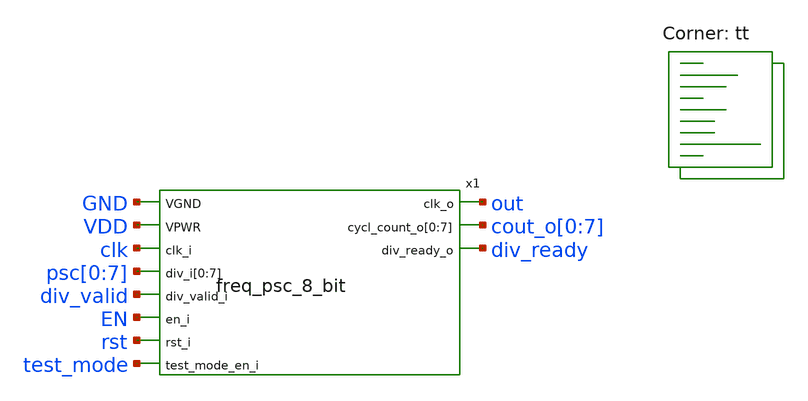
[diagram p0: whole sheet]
** sch_path: xschem/freq_psc_8_bit-tb.sch
**.subckt freq_psc_8_bit-tb
x1 GND VDD clk out cout_o[0] cout_o[1] cout_o[2] cout_o[3] cout_o[4] cout_o[5] cout_o[6] cout_o[7]
+ psc[0] psc[1] psc[2] psc[3] psc[4] psc[5] psc[6] psc[7] div_ready div_valid EN rst test_mode
+ freq_psc_8_bit
**** begin user architecture code



  .include ~/sky130_projects/sky130_its_biomedical_chip_research_2024/spice/clk_int_div.spice
  .param max_freq=100e6 period={1/max_freq} time_high={period/2}
  .param delay_vin1={time_high} delay_vin2={time_high*1.5}

  .option wnflag=1
  .option safecurrents

  Vvdd VDD GND dc 1.8
  Vrst rst GND pulse(0 1.8 {period*5} 1p 1p {time_high*5} {period*50})
  Vin1 clk GND pulse(0 1.8 {delay_vin1} 1p 1p {time_high} {period})

  Vdiv div_valid gnd pulse(0 1.8 {period*5} 1p 1p {period*50} {period*100})

  Vtest test_mode gnd dc 0
  Ven EN gnd dc 1.8

  Vpsc0  psc[0] gnd dc 0
  Vpsc1  psc[1] gnd dc 0
  Vpsc2  psc[2] gnd dc 1.8
  Vpsc3  psc[3] gnd dc 0
  Vpsc4  psc[4] gnd dc 0
  Vpsc5  psc[5] gnd dc 0
  Vpsc6  psc[6] gnd dc 0
  Vpsc7  psc[7] gnd dc 0

  .control
     reset
     save out clk psc[0] psc[1] psc[2] psc[3] psc[4] psc[5]
     +psc[6] psc[7] rst div_ready div_valid en test_mode

     tran 0.01n 2u uic
     remzerovec
     write freq_psc_8_bit-tb.raw
    quit 0
  .endc



 .lib $::SKYWATER_MODELS/sky130.lib.spice tt
.include $::SKYWATER_STDCELLS/sky130_fd_sc_hd.spice
.include $::SKYWATER_STDCELLS/sky130_ef_sc_hd__decap_12.spice
.include $::SKYWATER_STDCELLS/sky130_ef_sc_hd__fill_4.spice
.include $::SKYWATER_STDCELLS/sky130_ef_sc_hd__fill_8.spice
.include $::SKYWATER_STDCELLS/sky130_ef_sc_hd__fill_12.spice
.param mc_mm_switch = 0
.param mc_pr_switch = 0

**** end user architecture code
**.ends

* expanding   symbol:  freq_psc_8_bit.sym # of pins=11
** sym_path: xschem/freq_psc_8_bit.sym
** sch_path: xschem/freq_psc_8_bit.sch
.subckt freq_psc_8_bit VGND VPWR clk_i clk_o cycl_count_o[0] cycl_count_o[1] cycl_count_o[2]
+ cycl_count_o[3] cycl_count_o[4] cycl_count_o[5] cycl_count_o[6] cycl_count_o[7] div_i[0] div_i[1] div_i[2] div_i[3]
+ div_i[4] div_i[5] div_i[6] div_i[7] div_ready_o div_valid_i en_i rst_i test_mode_en_i
*.ipin VGND
*.ipin VPWR
*.ipin clk_i
*.opin clk_o
*.opin
*+ cycl_count_o[0],cycl_count_o[1],cycl_count_o[2],cycl_count_o[3],cycl_count_o[4],cycl_count_o[5],cycl_count_o[6],cycl_count_o[7]
*.ipin div_i[0],div_i[1],div_i[2],div_i[3],div_i[4],div_i[5],div_i[6],div_i[7]
*.opin div_ready_o
*.ipin div_valid_i
*.ipin en_i
*.ipin rst_i
*.ipin test_mode_en_i
.ends

.end
